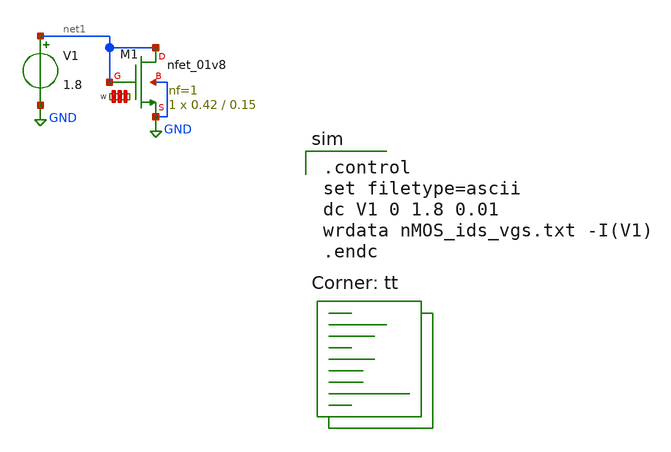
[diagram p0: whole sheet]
** sch_path: tutorial_1/nfetsat.sch
**.subckt nfetsat
XM1 net1 net1 GND GND sky130_fd_pr__nfet_01v8 L=0.15 W='0.42 * 1 ' nf=1 ad='int((nf+1)/2) * W / nf * 0.29'
+ as='int((nf+2)/2) * W / nf * 0.29' pd='2*int((nf+1)/2) * (W / nf + 0.29)' ps='2*int((nf+2)/2) * (W / nf + 0.29)'
+ nrd='0.29 / W ' nrs='0.29 / W ' sa=0 sb=0 sd=0 mult=1 m=1
V1 net1 GND 1.8
**** begin user architecture code

.control
set filetype=ascii
dc V1 0 1.8 0.01
wrdata nMOS_ids_vgs.txt -I(V1)
.endc

.lib $::SKYWATER_MODELS/sky130.lib.spice tt
**** end user architecture code
**.ends
.GLOBAL GND
.end
